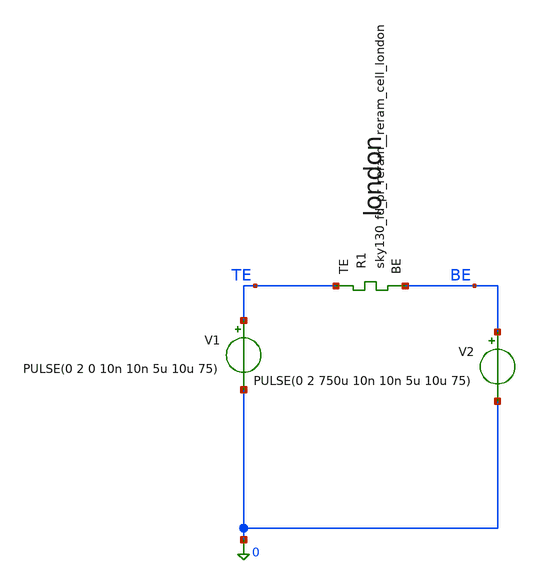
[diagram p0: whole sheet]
** sch_path: memristor_models/rram_london/tb_1R.sch
**.subckt tb_1R
XR1 TE BE sky130_fd_pr_reram__reram_cell_london
V1 TE 0 PULSE(0 2 0 10n 10n 5u 10u 75)
V2 BE 0 PULSE(0 2 750u 10n 10n 5u 10u 75)
**** begin user architecture code

** opencircuitdesign pdks install
.inc $::SKYWATER_MODELS/sky130_fd_pr_reram__reram_cell_london.spice



.option savecurrents
.tran 100n 1500u
.control
	save all
	run
	write tb_1R.raw
.endc



**** end user architecture code
**.ends
.end
